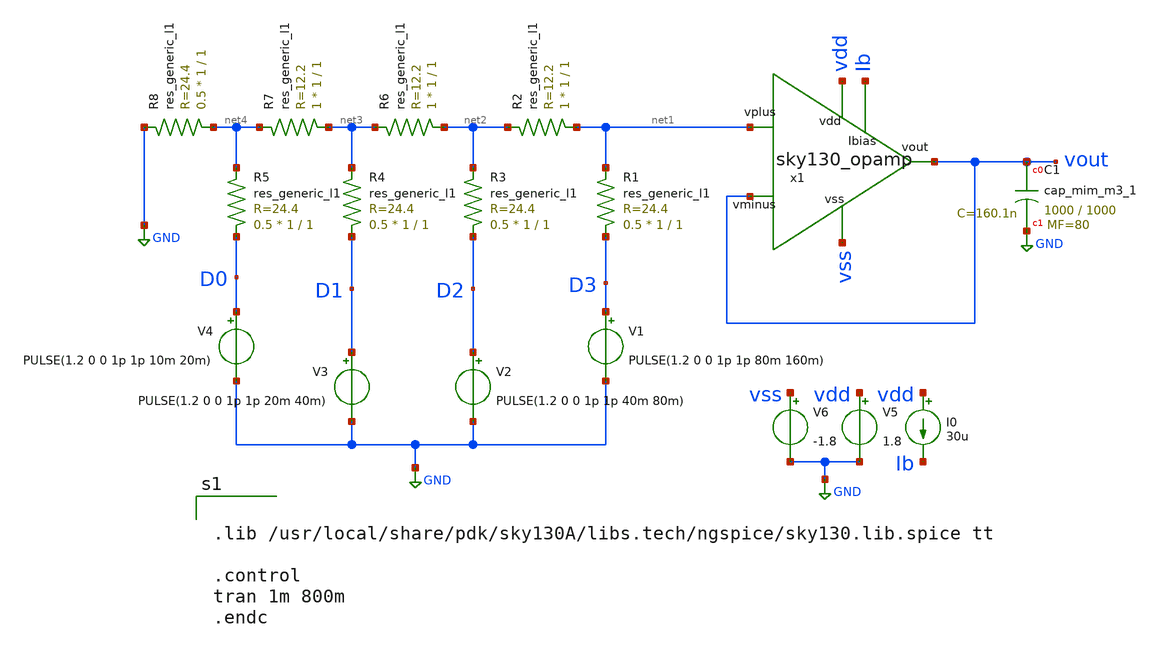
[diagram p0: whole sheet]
** sch_path: Digital to Analog Converter (DAC)/R-2R Ladder DAC/DAC_4bit.sch
**.subckt DAC_4bit
x1 vdd vout net1 vout Ib vss sky130_opamp
R1 D3 net1 sky130_fd_pr__res_generic_l1 W=1 L=1 m=0.5
R2 net1 net2 sky130_fd_pr__res_generic_l1 W=1 L=1 m=1
R3 D2 net2 sky130_fd_pr__res_generic_l1 W=1 L=1 m=0.5
R4 D1 net3 sky130_fd_pr__res_generic_l1 W=1 L=1 m=0.5
R5 D0 net4 sky130_fd_pr__res_generic_l1 W=1 L=1 m=0.5
R6 net2 net3 sky130_fd_pr__res_generic_l1 W=1 L=1 m=1
R7 net3 net4 sky130_fd_pr__res_generic_l1 W=1 L=1 m=1
R8 net4 GND sky130_fd_pr__res_generic_l1 W=1 L=1 m=0.5
V1 D3 GND PULSE(1.2 0 0 1p 1p 80m 160m)
V2 D2 GND PULSE(1.2 0 0 1p 1p 40m 80m)
V3 D1 GND PULSE(1.2 0 0 1p 1p 20m 40m)
V4 D0 GND PULSE(1.2 0 0 1p 1p 10m 20m)
V5 vdd GND 1.8
V6 vss GND -1.8
I0 vdd Ib 30u
XC1 vout GND sky130_fd_pr__cap_mim_m3_1 W=1000 L=1000 MF=80 m=80
**** begin user architecture code


.lib /usr/local/share/pdk/sky130A/libs.tech/ngspice/sky130.lib.spice tt

.control
tran 1m 800m
.endc


**** end user architecture code
**.ends

* expanding   symbol:  /home/rachtih/ADC trials/opamp/sky130_opamp.sym # of pins=6
** sym_path: Primitives/Operational Amplifier/Xschem Files/sky130_opamp.sym
** sch_path: Primitives/Operational Amplifier/Xschem Files/sky130_opamp.sch
.subckt sky130_opamp vdd vout vplus vminus Ibias vss
*.ipin Ibias
*.ipin vminus
*.ipin vplus
*.ipin vss
*.ipin vdd
*.opin vout
XM1 Ibias Ibias vss vss sky130_fd_pr__nfet_01v8 L=0.15 W=1 nf=1 ad='int((1 + 1)/2) * 1 / 1 * 0.29' as='int((1 + 2)/2) * 1 / 1 * 0.29'
+ pd='2*int((1 + 1)/2) * (1 / 1 + 0.29)' ps='2*int((1 + 2)/2) * (1 / 1 + 0.29)' nrd='0.29 / 1 ' nrs='0.29 / 1 '
+ sa=0 sb=0 sd=0 mult=1 m=1
XM2 net3 Ibias vss vss sky130_fd_pr__nfet_01v8 L=0.15 W=1 nf=1 ad='int((1 + 1)/2) * 1 / 1 * 0.29' as='int((1 + 2)/2) * 1 / 1 * 0.29'
+ pd='2*int((1 + 1)/2) * (1 / 1 + 0.29)' ps='2*int((1 + 2)/2) * (1 / 1 + 0.29)' nrd='0.29 / 1 ' nrs='0.29 / 1 '
+ sa=0 sb=0 sd=0 mult=1 m=1
XM3 net1 vminus net3 vss sky130_fd_pr__nfet_01v8 L=0.15 W=1 nf=1 ad='int((1 + 1)/2) * 1 / 1 * 0.29' as='int((1 + 2)/2) * 1 / 1 * 0.29'
+ pd='2*int((1 + 1)/2) * (1 / 1 + 0.29)' ps='2*int((1 + 2)/2) * (1 / 1 + 0.29)' nrd='0.29 / 1 ' nrs='0.29 / 1 '
+ sa=0 sb=0 sd=0 mult=1 m=1
XM4 net2 vplus net3 vss sky130_fd_pr__nfet_01v8 L=0.15 W=1 nf=1 ad='int((1 + 1)/2) * 1 / 1 * 0.29' as='int((1 + 2)/2) * 1 / 1 * 0.29'
+ pd='2*int((1 + 1)/2) * (1 / 1 + 0.29)' ps='2*int((1 + 2)/2) * (1 / 1 + 0.29)' nrd='0.29 / 1 ' nrs='0.29 / 1 '
+ sa=0 sb=0 sd=0 mult=1 m=1
XM5 vout Ibias vss vss sky130_fd_pr__nfet_01v8 L=0.15 W=1 nf=1 ad='int((1 + 1)/2) * 1 / 1 * 0.29' as='int((1 + 2)/2) * 1 / 1 * 0.29'
+ pd='2*int((1 + 1)/2) * (1 / 1 + 0.29)' ps='2*int((1 + 2)/2) * (1 / 1 + 0.29)' nrd='0.29 / 1 ' nrs='0.29 / 1 '
+ sa=0 sb=0 sd=0 mult=1 m=1
XM6 net2 net1 vdd vdd sky130_fd_pr__pfet_01v8 L=0.15 W=1 nf=1 ad='int((1 + 1)/2) * 1 / 1 * 0.29' as='int((1 + 2)/2) * 1 / 1 * 0.29'
+ pd='2*int((1 + 1)/2) * (1 / 1 + 0.29)' ps='2*int((1 + 2)/2) * (1 / 1 + 0.29)' nrd='0.29 / 1 ' nrs='0.29 / 1 '
+ sa=0 sb=0 sd=0 mult=1 m=1
XM7 net1 net1 vdd vdd sky130_fd_pr__pfet_01v8 L=0.15 W=1 nf=1 ad='int((1 + 1)/2) * 1 / 1 * 0.29' as='int((1 + 2)/2) * 1 / 1 * 0.29'
+ pd='2*int((1 + 1)/2) * (1 / 1 + 0.29)' ps='2*int((1 + 2)/2) * (1 / 1 + 0.29)' nrd='0.29 / 1 ' nrs='0.29 / 1 '
+ sa=0 sb=0 sd=0 mult=1 m=1
XM8 vout net2 vdd vdd sky130_fd_pr__pfet_01v8 L=0.15 W=1 nf=1 ad='int((1 + 1)/2) * 1 / 1 * 0.29' as='int((1 + 2)/2) * 1 / 1 * 0.29'
+ pd='2*int((1 + 1)/2) * (1 / 1 + 0.29)' ps='2*int((1 + 2)/2) * (1 / 1 + 0.29)' nrd='0.29 / 1 ' nrs='0.29 / 1 '
+ sa=0 sb=0 sd=0 mult=1 m=1
C1 net4 vout 2.7p m=1
R1 net2 net4 50 m=1
.ends

.GLOBAL GND
.end
